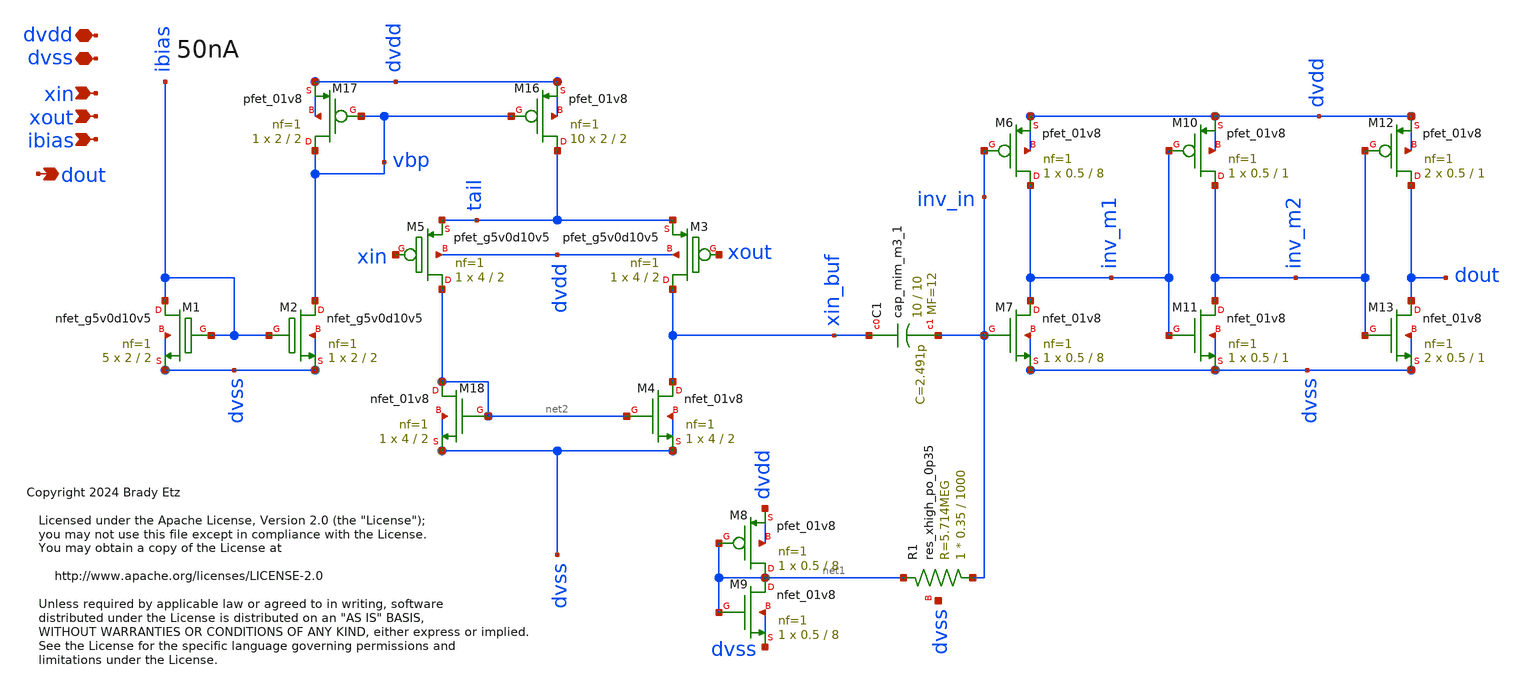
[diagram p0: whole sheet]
** sch_path: xschem/dout_amp.sch
* Copyright 2024 Brady Etz
* Licensed under the Apache License, Version 2.0 (the "License");
**.subckt dout_amp xin dvdd dvss dout ibias xout
*.ipin xin
*.iopin dvdd
*.iopin dvss
*.opin dout
*.ipin ibias
*.ipin xout
XM1 ibias ibias dvss dvss sky130_fd_pr__nfet_g5v0d10v5 L=2 W=2 nf=1 ad='int((nf+1)/2) * W/nf * 0.29'
+ as='int((nf+2)/2) * W/nf * 0.29' pd='2*int((nf+1)/2) * (W/nf + 0.29)' ps='2*int((nf+2)/2) * (W/nf + 0.29)'
+ nrd='0.29 / W' nrs='0.29 / W' sa=0 sb=0 sd=0 mult=5 m=5
XM2 vbp ibias dvss dvss sky130_fd_pr__nfet_g5v0d10v5 L=2 W=2 nf=1 ad='int((nf+1)/2) * W/nf * 0.29' as='int((nf+2)/2) * W/nf * 0.29'
+ pd='2*int((nf+1)/2) * (W/nf + 0.29)' ps='2*int((nf+2)/2) * (W/nf + 0.29)' nrd='0.29 / W' nrs='0.29 / W'
+ sa=0 sb=0 sd=0 mult=1 m=1
XM5 net2 xin tail dvdd sky130_fd_pr__pfet_g5v0d10v5 L=2 W=4 nf=1 ad='int((nf+1)/2) * W/nf * 0.29' as='int((nf+2)/2) * W/nf * 0.29'
+ pd='2*int((nf+1)/2) * (W/nf + 0.29)' ps='2*int((nf+2)/2) * (W/nf + 0.29)' nrd='0.29 / W' nrs='0.29 / W'
+ sa=0 sb=0 sd=0 mult=1 m=1
XC1 xin_buf inv_in sky130_fd_pr__cap_mim_m3_1 W=10 L=10 MF=12 m=12
XM6 inv_m1 inv_in dvdd dvdd sky130_fd_pr__pfet_01v8 L=8 W=0.5 nf=1 ad='int((nf+1)/2) * W/nf * 0.29' as='int((nf+2)/2) * W/nf * 0.29'
+ pd='2*int((nf+1)/2) * (W/nf + 0.29)' ps='2*int((nf+2)/2) * (W/nf + 0.29)' nrd='0.29 / W' nrs='0.29 / W'
+ sa=0 sb=0 sd=0 mult=1 m=1
XM7 inv_m1 inv_in dvss dvss sky130_fd_pr__nfet_01v8 L=8 W=0.5 nf=1 ad='int((nf+1)/2) * W/nf * 0.29' as='int((nf+2)/2) * W/nf * 0.29'
+ pd='2*int((nf+1)/2) * (W/nf + 0.29)' ps='2*int((nf+2)/2) * (W/nf + 0.29)' nrd='0.29 / W' nrs='0.29 / W'
+ sa=0 sb=0 sd=0 mult=1 m=1
XM8 net1 net1 dvdd dvdd sky130_fd_pr__pfet_01v8 L=8 W=0.5 nf=1 ad='int((nf+1)/2) * W/nf * 0.29' as='int((nf+2)/2) * W/nf * 0.29'
+ pd='2*int((nf+1)/2) * (W/nf + 0.29)' ps='2*int((nf+2)/2) * (W/nf + 0.29)' nrd='0.29 / W' nrs='0.29 / W'
+ sa=0 sb=0 sd=0 mult=1 m=1
XM9 net1 net1 dvss dvss sky130_fd_pr__nfet_01v8 L=8 W=0.5 nf=1 ad='int((nf+1)/2) * W/nf * 0.29' as='int((nf+2)/2) * W/nf * 0.29'
+ pd='2*int((nf+1)/2) * (W/nf + 0.29)' ps='2*int((nf+2)/2) * (W/nf + 0.29)' nrd='0.29 / W' nrs='0.29 / W'
+ sa=0 sb=0 sd=0 mult=1 m=1
XR1 inv_in net1 dvss sky130_fd_pr__res_xhigh_po_0p35 L=1000 mult=1 m=1
XM10 inv_m2 inv_m1 dvdd dvdd sky130_fd_pr__pfet_01v8 L=1 W=0.5 nf=1 ad='int((nf+1)/2) * W/nf * 0.29'
+ as='int((nf+2)/2) * W/nf * 0.29' pd='2*int((nf+1)/2) * (W/nf + 0.29)' ps='2*int((nf+2)/2) * (W/nf + 0.29)'
+ nrd='0.29 / W' nrs='0.29 / W' sa=0 sb=0 sd=0 mult=1 m=1
XM11 inv_m2 inv_m1 dvss dvss sky130_fd_pr__nfet_01v8 L=1 W=0.5 nf=1 ad='int((nf+1)/2) * W/nf * 0.29'
+ as='int((nf+2)/2) * W/nf * 0.29' pd='2*int((nf+1)/2) * (W/nf + 0.29)' ps='2*int((nf+2)/2) * (W/nf + 0.29)'
+ nrd='0.29 / W' nrs='0.29 / W' sa=0 sb=0 sd=0 mult=1 m=1
XM12 dout inv_m2 dvdd dvdd sky130_fd_pr__pfet_01v8 L=1 W=0.5 nf=1 ad='int((nf+1)/2) * W/nf * 0.29' as='int((nf+2)/2) * W/nf * 0.29'
+ pd='2*int((nf+1)/2) * (W/nf + 0.29)' ps='2*int((nf+2)/2) * (W/nf + 0.29)' nrd='0.29 / W' nrs='0.29 / W'
+ sa=0 sb=0 sd=0 mult=2 m=2
XM13 dout inv_m2 dvss dvss sky130_fd_pr__nfet_01v8 L=1 W=0.5 nf=1 ad='int((nf+1)/2) * W/nf * 0.29' as='int((nf+2)/2) * W/nf * 0.29'
+ pd='2*int((nf+1)/2) * (W/nf + 0.29)' ps='2*int((nf+2)/2) * (W/nf + 0.29)' nrd='0.29 / W' nrs='0.29 / W'
+ sa=0 sb=0 sd=0 mult=2 m=2
XM16 tail vbp dvdd dvdd sky130_fd_pr__pfet_01v8 L=2 W=2 nf=1 ad='int((nf+1)/2) * W/nf * 0.29' as='int((nf+2)/2) * W/nf * 0.29'
+ pd='2*int((nf+1)/2) * (W/nf + 0.29)' ps='2*int((nf+2)/2) * (W/nf + 0.29)' nrd='0.29 / W' nrs='0.29 / W'
+ sa=0 sb=0 sd=0 mult=10 m=10
XM17 vbp vbp dvdd dvdd sky130_fd_pr__pfet_01v8 L=2 W=2 nf=1 ad='int((nf+1)/2) * W/nf * 0.29' as='int((nf+2)/2) * W/nf * 0.29'
+ pd='2*int((nf+1)/2) * (W/nf + 0.29)' ps='2*int((nf+2)/2) * (W/nf + 0.29)' nrd='0.29 / W' nrs='0.29 / W'
+ sa=0 sb=0 sd=0 mult=1 m=1
XM3 xin_buf xout tail dvdd sky130_fd_pr__pfet_g5v0d10v5 L=2 W=4 nf=1 ad='int((nf+1)/2) * W/nf * 0.29'
+ as='int((nf+2)/2) * W/nf * 0.29' pd='2*int((nf+1)/2) * (W/nf + 0.29)' ps='2*int((nf+2)/2) * (W/nf + 0.29)'
+ nrd='0.29 / W' nrs='0.29 / W' sa=0 sb=0 sd=0 mult=1 m=1
XM4 xin_buf net2 dvss dvss sky130_fd_pr__nfet_01v8 L=2 W=4 nf=1 ad='int((nf+1)/2) * W/nf * 0.29' as='int((nf+2)/2) * W/nf * 0.29'
+ pd='2*int((nf+1)/2) * (W/nf + 0.29)' ps='2*int((nf+2)/2) * (W/nf + 0.29)' nrd='0.29 / W' nrs='0.29 / W'
+ sa=0 sb=0 sd=0 mult=1 m=1
XM18 net2 net2 dvss dvss sky130_fd_pr__nfet_01v8 L=2 W=4 nf=1 ad='int((nf+1)/2) * W/nf * 0.29' as='int((nf+2)/2) * W/nf * 0.29'
+ pd='2*int((nf+1)/2) * (W/nf + 0.29)' ps='2*int((nf+2)/2) * (W/nf + 0.29)' nrd='0.29 / W' nrs='0.29 / W'
+ sa=0 sb=0 sd=0 mult=1 m=1
**.ends
.end
